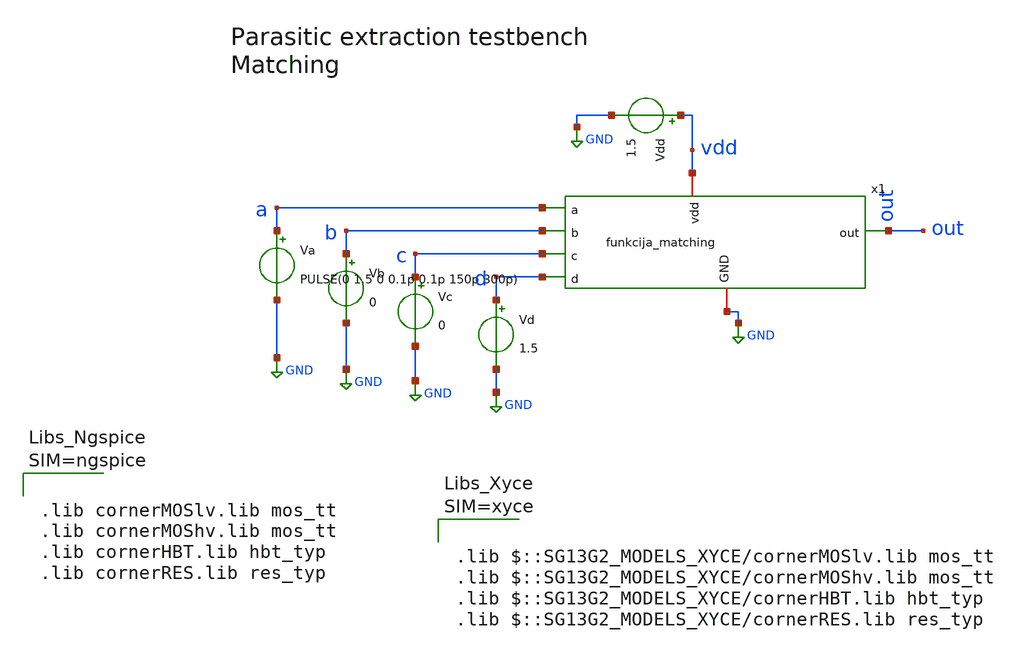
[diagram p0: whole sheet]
** sch_path: projekat/slucaj_2/pex/testbench/tb_tran_matching.sch
**.subckt tb_tran_matching
Va a GND PULSE(0 1.5 0 0.1p 0.1p 150p 300p)
Vb b GND 0
Vc c GND 0
Vd d GND 1.5
Vdd vdd GND 1.5
x1 vdd out d a c b GND funkcija_matching
**** begin user architecture code



.lib cornerMOSlv.lib mos_tt
.lib cornerMOShv.lib mos_tt
.lib cornerHBT.lib hbt_typ
.lib cornerRES.lib res_typ








.include /home/Nikola.Jankovic/projekat/slucaj_2/pex/layout/funkcija_matching.spice
.tran 0.1p 800p

.control
  save all
  run

  meas tran tr_out TRIG v(out) VAL=0.15 RISE=2 TARG v(out) VAL=1.35 RISE=2
  meas tran tf_out TRIG v(out) VAL=1.35 FALL=2 TARG v(out) VAL=0.15 FALL=2

  plot v(a)+4.5 v(b)+3 v(c)+1.5 v(out)
  wrdata /home/Nikola.Jankovic/projekat/slucaj_2/pex/python/odziv_match.txt v(a) v(out)
  print tr_out tf_out
.endc

**** end user architecture code
**.ends
.GLOBAL GND
.end
